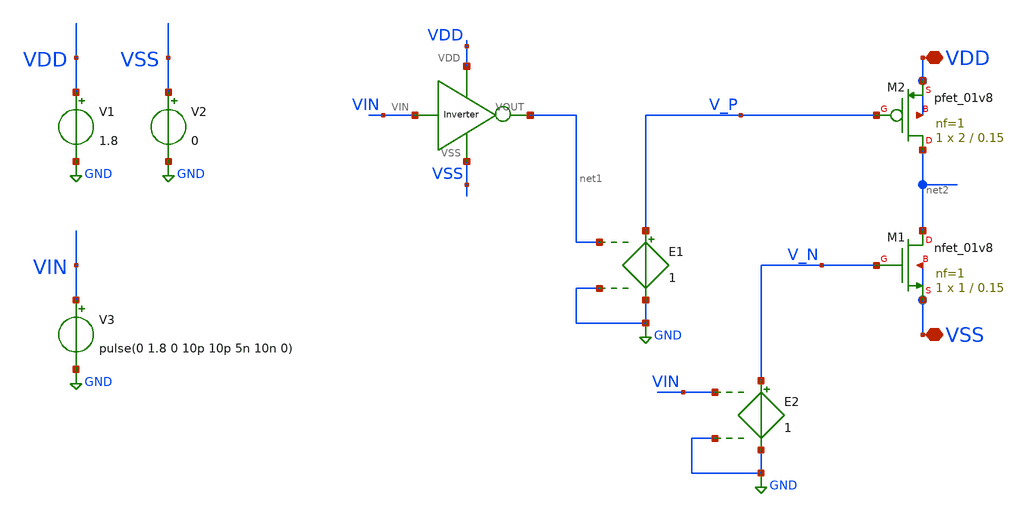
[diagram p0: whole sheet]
** sch_path: xschem/DC_DC_Converter_xschem/OTHERS/DC_DC_Converter0/Open_Loop_Buck_converter.sch
**.subckt Open_Loop_Buck_converter VDD VSS
*.iopin VDD
*.iopin VSS
V1 VDD GND 1.8
V2 VSS GND 0
V3 VIN GND pulse(0 1.8 0 10p 10p 5n 10n 0)
X1 VIN net1 VDD VSS Inverter
E1 V_P GND net1 GND 1
XM1 net2 V_N VSS VSS sky130_fd_pr__nfet_01v8 L=0.15 W=1 nf=1 ad='int((nf+1)/2) * W/nf * 0.29' as='int((nf+2)/2) * W/nf * 0.29'
+ pd='2*int((nf+1)/2) * (W/nf + 0.29)' ps='2*int((nf+2)/2) * (W/nf + 0.29)' nrd='0.29 / W' nrs='0.29 / W'
+ sa=0 sb=0 sd=0 mult=1 m=1
XM2 net2 V_P VDD VDD sky130_fd_pr__pfet_01v8 L=0.15 W=2 nf=1 ad='int((nf+1)/2) * W/nf * 0.29' as='int((nf+2)/2) * W/nf * 0.29'
+ pd='2*int((nf+1)/2) * (W/nf + 0.29)' ps='2*int((nf+2)/2) * (W/nf + 0.29)' nrd='0.29 / W' nrs='0.29 / W'
+ sa=0 sb=0 sd=0 mult=1 m=1
E2 V_N GND VIN GND 1
**** begin user architecture code


.control

tran 1n 50n
plot v(VIN) v(VOUT)
.endc



** opencircuitdesign pdks install
.lib $::SKYWATER_MODELS/sky130.lib.spice tt


**** end user architecture code
**.ends
.GLOBAL GND
.end
